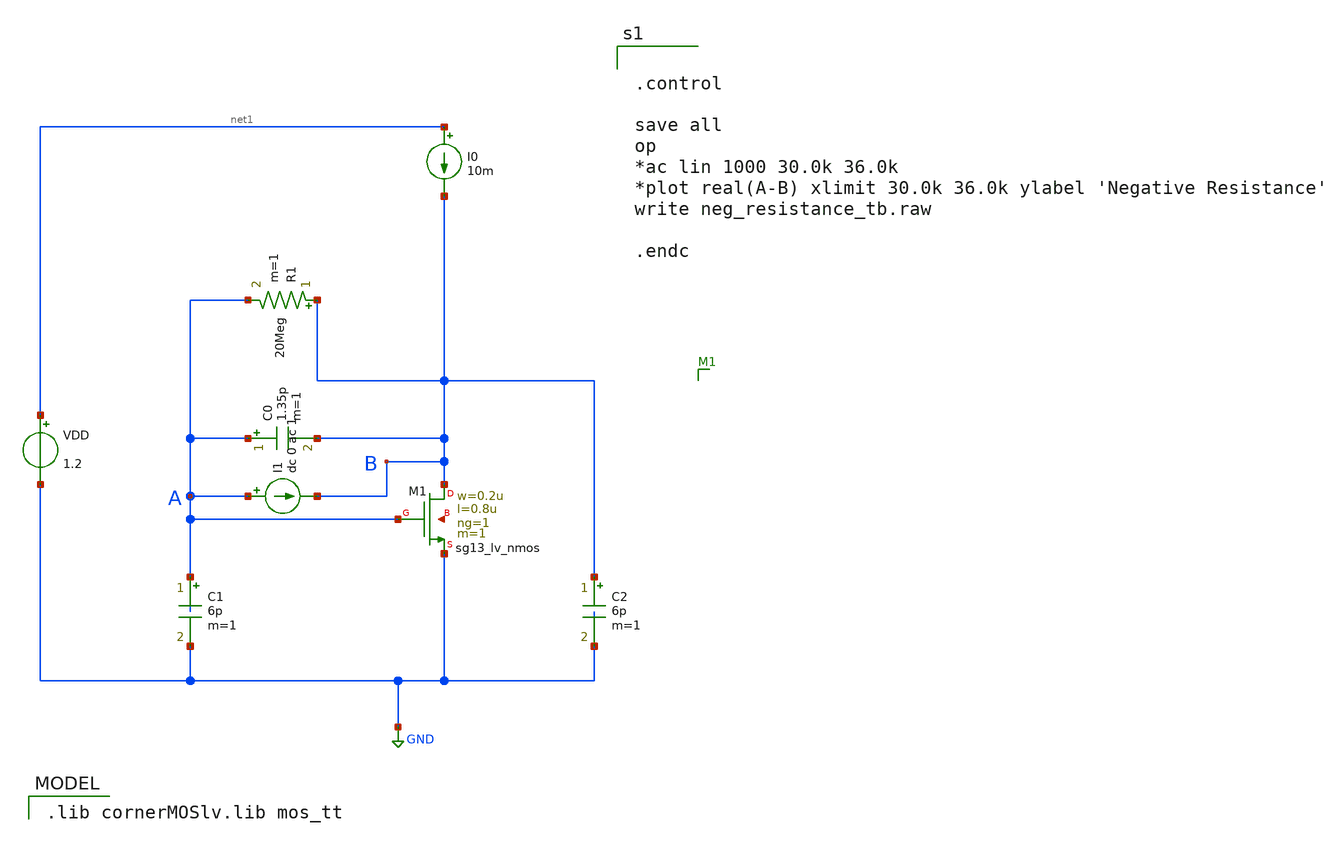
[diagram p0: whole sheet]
** sch_path: neg_resistance_tb.sch
**.subckt neg_resistance_tb
XM1 B A GND net2 sg13_lv_nmos w=0.2u l=0.8u ng=1 m=1 mm_ok=1
C1 A GND 6p m=1
C2 B GND 6p m=1
C0 A B 1.35p m=1
I0 net1 B 10m
VDD net1 GND 1.2
R1 B A 20Meg m=1
I1 A B dc 0 ac 1
**** begin user architecture code


.control

save all
op
*ac lin 1000 30.0k 36.0k
*plot real(A-B) xlimit 30.0k 36.0k ylabel 'Negative Resistance'
write neg_resistance_tb.raw

.endc


 .lib cornerMOSlv.lib mos_tt

**** end user architecture code
**.ends
.GLOBAL GND
.end
